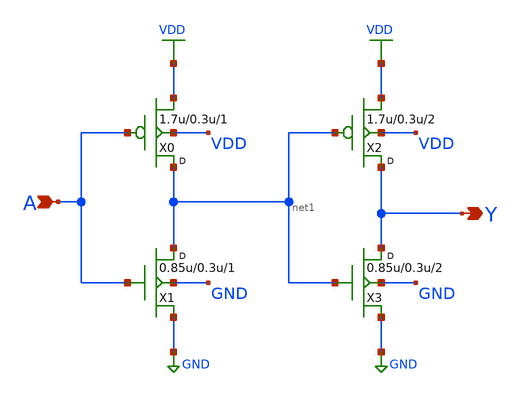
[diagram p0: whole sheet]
** sch_path: openfasoc/common/platforms/gf180mcuosu9Tbuf2/gf180mcu_osu_sc_buf_2.sch
**.subckt gf180mcu_osu_sc_buf_2 A Y
*.ipin A
*.opin Y
X0 net1 A VDD VDD pmos_3p3 w=1.7u l=0.3u m=1
X1 net1 A GND GND nmos_3p3 w=0.85u l=0.3u m=1
X2 Y net1 VDD VDD pmos_3p3 w=1.7u l=0.3u m=2
X3 Y net1 GND GND nmos_3p3 w=0.85u l=0.3u m=2
**.ends
.GLOBAL VDD
.GLOBAL GND
.end
